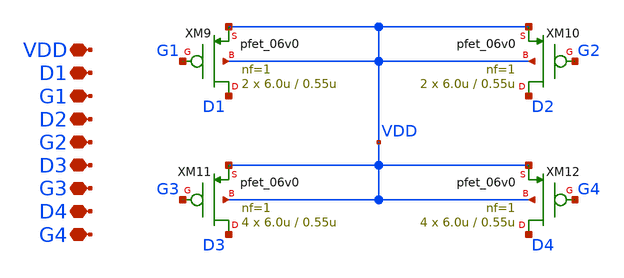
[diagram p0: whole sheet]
** sch_path: designs/libs/core_single-fet/pfet-com/pfet-com.sch
**.subckt pfet-com VDD D1 G1 D2 G2 D3 G3 G4 D4
*.iopin VDD
*.iopin D1
*.iopin G1
*.iopin D2
*.iopin G2
*.iopin D3
*.iopin G3
*.iopin G4
*.iopin D4
XM9 D1 G1 VDD VDD pfet_06v0 L=0.55u W=6.0u nf=1 ad='int((nf+1)/2) * W/nf * 0.18u' as='int((nf+2)/2) * W/nf * 0.18u'
+ pd='2*int((nf+1)/2) * (W/nf + 0.18u)' ps='2*int((nf+2)/2) * (W/nf + 0.18u)' nrd='0.18u / W' nrs='0.18u / W'
+ sa=0 sb=0 sd=0 m=2
XM10 D2 G2 VDD VDD pfet_06v0 L=0.55u W=6.0u nf=1 ad='int((nf+1)/2) * W/nf * 0.18u' as='int((nf+2)/2) * W/nf * 0.18u'
+ pd='2*int((nf+1)/2) * (W/nf + 0.18u)' ps='2*int((nf+2)/2) * (W/nf + 0.18u)' nrd='0.18u / W' nrs='0.18u / W'
+ sa=0 sb=0 sd=0 m=2
XM11 D3 G3 VDD VDD pfet_06v0 L=0.55u W=6.0u nf=1 ad='int((nf+1)/2) * W/nf * 0.18u' as='int((nf+2)/2) * W/nf * 0.18u'
+ pd='2*int((nf+1)/2) * (W/nf + 0.18u)' ps='2*int((nf+2)/2) * (W/nf + 0.18u)' nrd='0.18u / W' nrs='0.18u / W'
+ sa=0 sb=0 sd=0 m=4
XM12 D4 G4 VDD VDD pfet_06v0 L=0.55u W=6.0u nf=1 ad='int((nf+1)/2) * W/nf * 0.18u' as='int((nf+2)/2) * W/nf * 0.18u'
+ pd='2*int((nf+1)/2) * (W/nf + 0.18u)' ps='2*int((nf+2)/2) * (W/nf + 0.18u)' nrd='0.18u / W' nrs='0.18u / W'
+ sa=0 sb=0 sd=0 m=4
**.ends
.end
